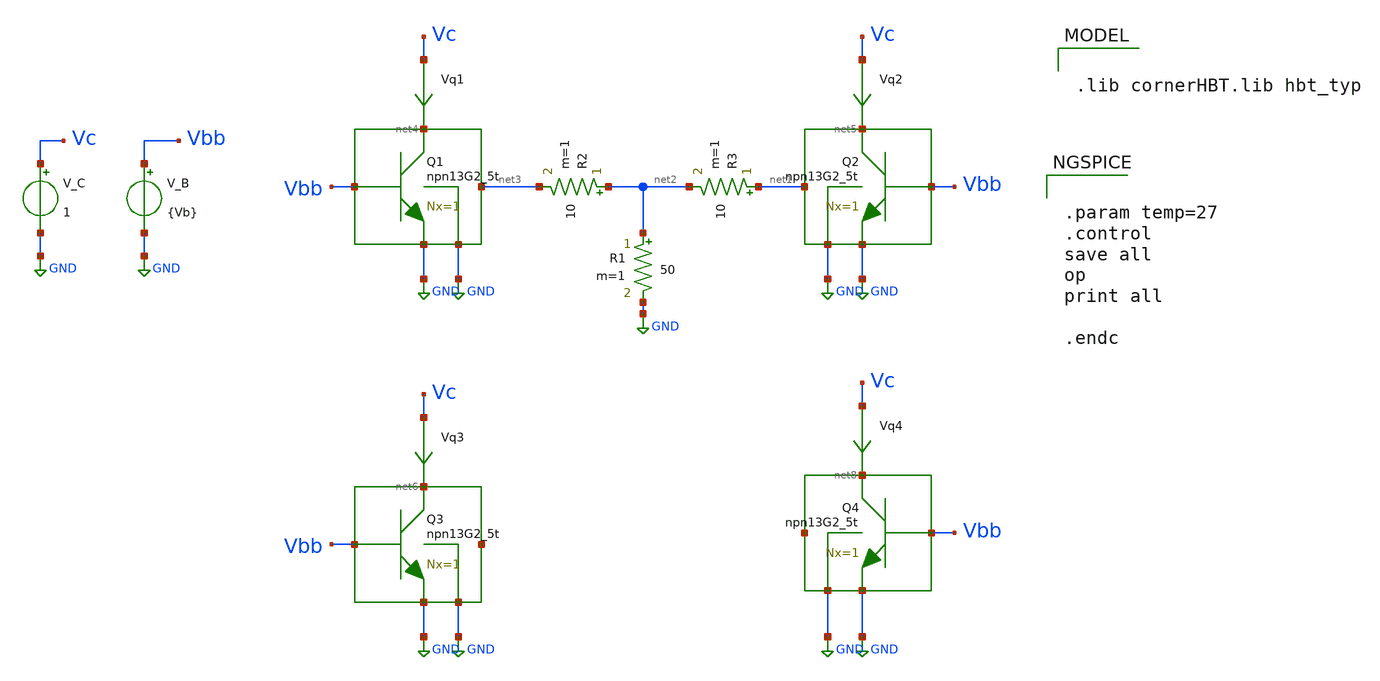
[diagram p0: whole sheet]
** sch_path: ihp-sg13g2/libs.tech/xschem/sg13g2_tests_xyce/npn13G2_5t_coupling_err.sch
**.subckt npn13G2_5t_coupling_err
XQ1 net4 Vbb GND GND net3 npn13G2_5t Nx=1 mm_ok=1
R1 net2 GND 50 m=1
XQ2 net5 Vbb GND GND net1 npn13G2_5t Nx=1 mm_ok=1
R2 net2 net3 10 m=1
R3 net1 net2 10 m=1
XQ3 net6 Vbb GND GND net7 npn13G2_5t Nx=1 mm_ok=1
XQ4 net8 Vbb GND GND net9 npn13G2_5t Nx=1 mm_ok=1
V_C Vc GND 1
V_B Vbb GND {Vb}
Vq3 Vc net6 0
.save i(vq3)
Vq4 Vc net8 0
.save i(vq4)
Vq1 Vc net4 0
.save i(vq1)
Vq2 Vc net5 0
.save i(vq2)
**** begin user architecture code

.lib cornerHBT.lib hbt_typ



.param temp=27
.control
save all
op
print all

.endc


**** end user architecture code
**.ends
.GLOBAL GND
.end
